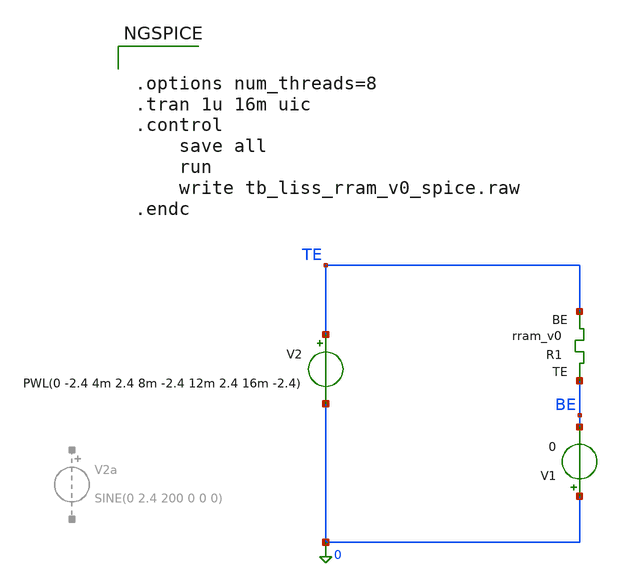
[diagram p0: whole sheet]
** sch_path: memristor_models/wellposed_spice/tb_liss_rram_v0_spice.sch
**.subckt tb_liss_rram_v0_spice
XR1 BE TE rram_v0
V1 0 BE 0
V2 TE 0 PWL(0 -2.4 4m 2.4 8m -2.4 12m 2.4 16m -2.4)
**** begin user architecture code


.options num_threads=8
.tran 1u 16m uic
.control
	save all
	run
	write tb_liss_rram_v0_spice.raw
.endc




** opencircuitdesign pdks install
.inc /home/alex/Desktop/EDA/SNN_IPN/memristor_models/wellposed_spice/wllpsd.spice

**** end user architecture code
**.ends
.end
